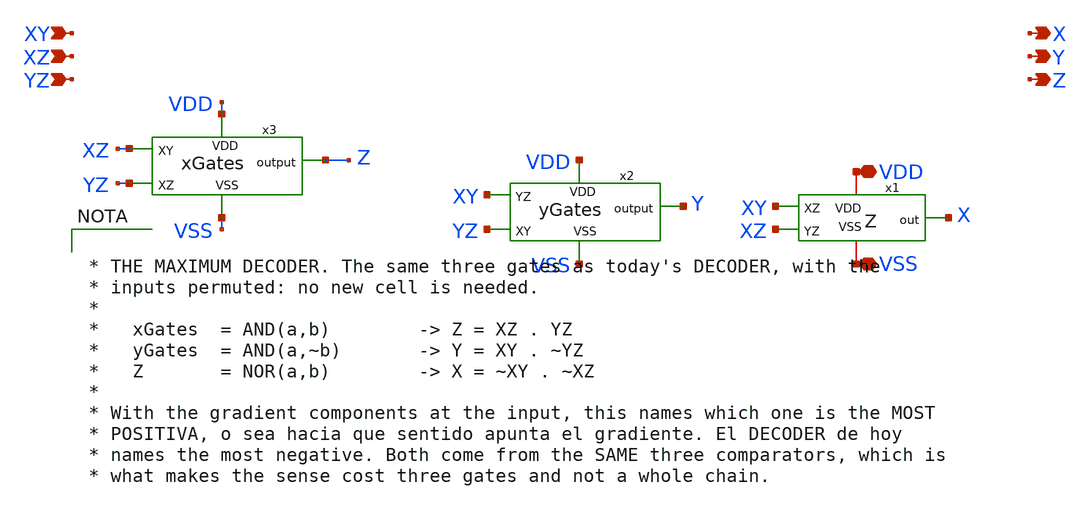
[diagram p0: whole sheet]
** sch_path: FINAL/XSCHEM_v2/DECODER_MAX.sch
**.subckt DECODER_MAX XY XZ YZ VDD VSS X Y Z
*.ipin XY
*.ipin XZ
*.ipin YZ
*.iopin VDD
*.iopin VSS
*.opin X
*.opin Y
*.opin Z
x3 VDD XZ Z YZ VSS xGates
x2 XY YZ VDD Y VSS yGates
x1 VSS VDD XY XZ X Z
**** begin user architecture code


* THE MAXIMUM DECODER. The same three gates as today's DECODER, with the
* inputs permuted: no new cell is needed.
*
*   xGates  = AND(a,b)        -> Z = XZ . YZ
*   yGates  = AND(a,~b)       -> Y = XY . ~YZ
*   Z       = NOR(a,b)        -> X = ~XY . ~XZ
*
* With the gradient components at the input, this names which one is the MOST
* POSITIVA, o sea hacia que sentido apunta el gradiente. El DECODER de hoy
* names the most negative. Both come from the SAME three comparators, which is
* what makes the sense cost three gates and not a whole chain.


**** end user architecture code
**.ends
.end
